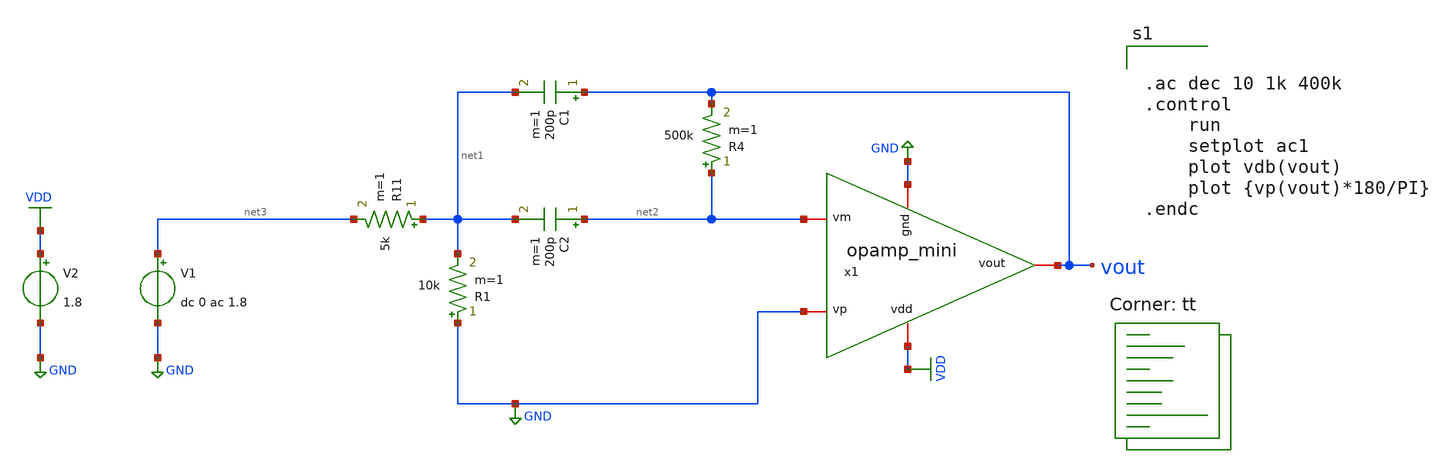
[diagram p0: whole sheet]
** sch_path: BandpassFilter/tb_bpf.sch
**.subckt tb_bpf
R11 net1 net3 5k m=1
R4 net2 vout 500k m=1
C1 vout net1 200p m=1
C2 net2 net1 200p m=1
R1 GND net1 10k m=1
V1 net3 GND dc 0 ac 1.8
V2 VDD GND 1.8
x1 VDD vout net2 GND GND opamp_mini
**** begin user architecture code


.ac dec 10 1k 400k
.control
	run
	setplot ac1
	plot vdb(vout)
	plot {vp(vout)*180/PI}
.endc


.lib $::SKYWATER_MODELS/sky130.lib.spice tt
**** end user architecture code
**.ends

* expanding   symbol:  /home/alex/Desktop/EDA/SNN_IPN/OPAMP/opamp_mini.sym # of pins=5
** sym_path: OPAMP/opamp_mini.sym
** sch_path: OPAMP/opamp_mini.sch
.subckt opamp_mini vdd vout vm vp gnd
*.iopin vdd
*.iopin gnd
*.iopin vout
*.iopin vm
*.iopin vp
XM1 vout vb2 vdd vdd sky130_fd_pr__pfet_01v8 L=0.8 W=4 nf=1 ad='int((nf+1)/2) * W/nf * 0.29' as='int((nf+2)/2) * W/nf * 0.29'
+ pd='2*int((nf+1)/2) * (W/nf + 0.29)' ps='2*int((nf+2)/2) * (W/nf + 0.29)' nrd='0.29 / W' nrs='0.29 / W'
+ sa=0 sb=0 sd=0 mult=1 m=1
XM2 vb2 vb2 vdd vdd sky130_fd_pr__pfet_01v8 L=0.8 W=4 nf=1 ad='int((nf+1)/2) * W/nf * 0.29' as='int((nf+2)/2) * W/nf * 0.29'
+ pd='2*int((nf+1)/2) * (W/nf + 0.29)' ps='2*int((nf+2)/2) * (W/nf + 0.29)' nrd='0.29 / W' nrs='0.29 / W'
+ sa=0 sb=0 sd=0 mult=1 m=1
XM3 vb2 vp net1 gnd sky130_fd_pr__nfet_01v8 L=0.3 W=2 nf=1 ad='int((nf+1)/2) * W/nf * 0.29' as='int((nf+2)/2) * W/nf * 0.29'
+ pd='2*int((nf+1)/2) * (W/nf + 0.29)' ps='2*int((nf+2)/2) * (W/nf + 0.29)' nrd='0.29 / W' nrs='0.29 / W'
+ sa=0 sb=0 sd=0 mult=1 m=1
XM4 vout vm net1 gnd sky130_fd_pr__nfet_01v8 L=0.3 W=2 nf=1 ad='int((nf+1)/2) * W/nf * 0.29' as='int((nf+2)/2) * W/nf * 0.29'
+ pd='2*int((nf+1)/2) * (W/nf + 0.29)' ps='2*int((nf+2)/2) * (W/nf + 0.29)' nrd='0.29 / W' nrs='0.29 / W'
+ sa=0 sb=0 sd=0 mult=1 m=1
XM5 net1 vb1 gnd gnd sky130_fd_pr__nfet_01v8 L=1.2 W=0.7 nf=1 ad='int((nf+1)/2) * W/nf * 0.29' as='int((nf+2)/2) * W/nf * 0.29'
+ pd='2*int((nf+1)/2) * (W/nf + 0.29)' ps='2*int((nf+2)/2) * (W/nf + 0.29)' nrd='0.29 / W' nrs='0.29 / W'
+ sa=0 sb=0 sd=0 mult=1 m=1
R1 vdd vb1 1k m=1
R2 vb1 gnd 1k m=1
.ends

.GLOBAL VDD
.GLOBAL GND
.end
